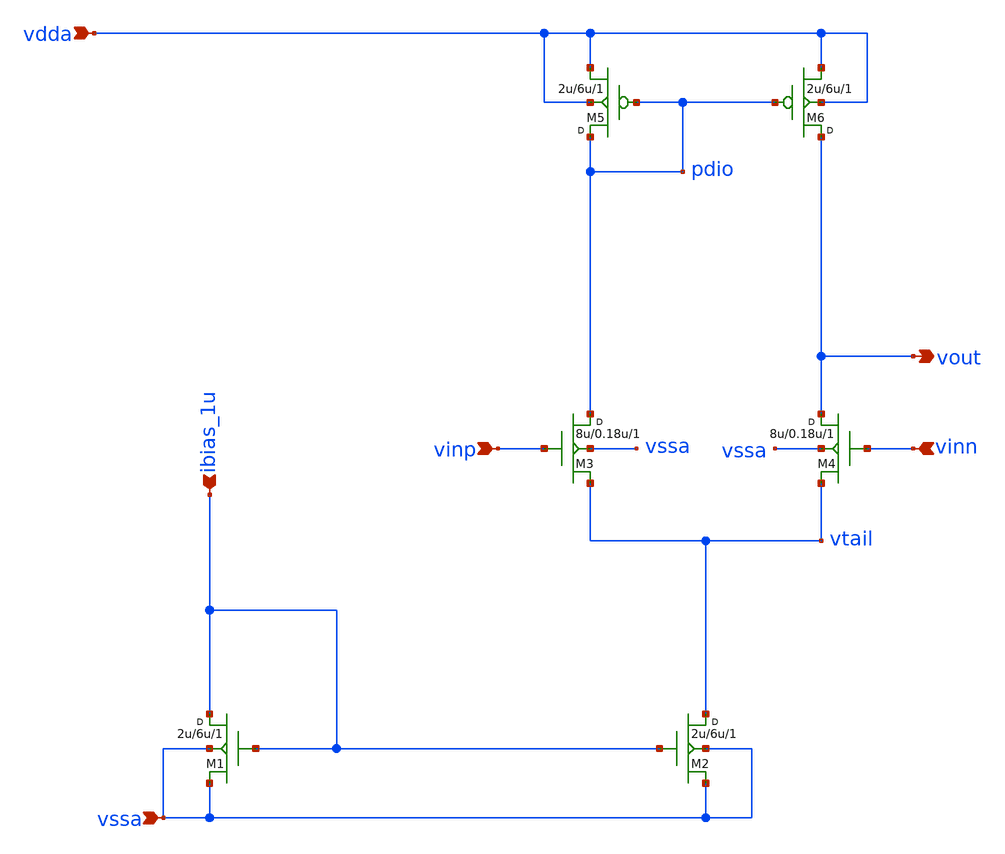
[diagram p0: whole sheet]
** sch_path: Running_closed_loop_stability_analysis_in_ngspice_through_xschem/OTA.sch
**.subckt OTA vdda vssa ibias_1u vinn vinp vout
*.ipin vdda
*.ipin vssa
*.ipin ibias_1u
*.ipin vinn
*.ipin vinp
*.opin vout
M6 vout pdio vdda vdda pmosx w=2u l=6u m=1
M5 pdio pdio vdda vdda pmosx w=2u l=6u m=1
M3 pdio vinp vtail vssa nmos w=8u l=0.18u m=1
M4 vout vinn vtail vssa nmos w=8u l=0.18u m=1
M2 vtail ibias_1u vssa vssa nmos w=2u l=6u m=1
M1 ibias_1u ibias_1u vssa vssa nmos w=2u l=6u m=1
**.ends
.end
